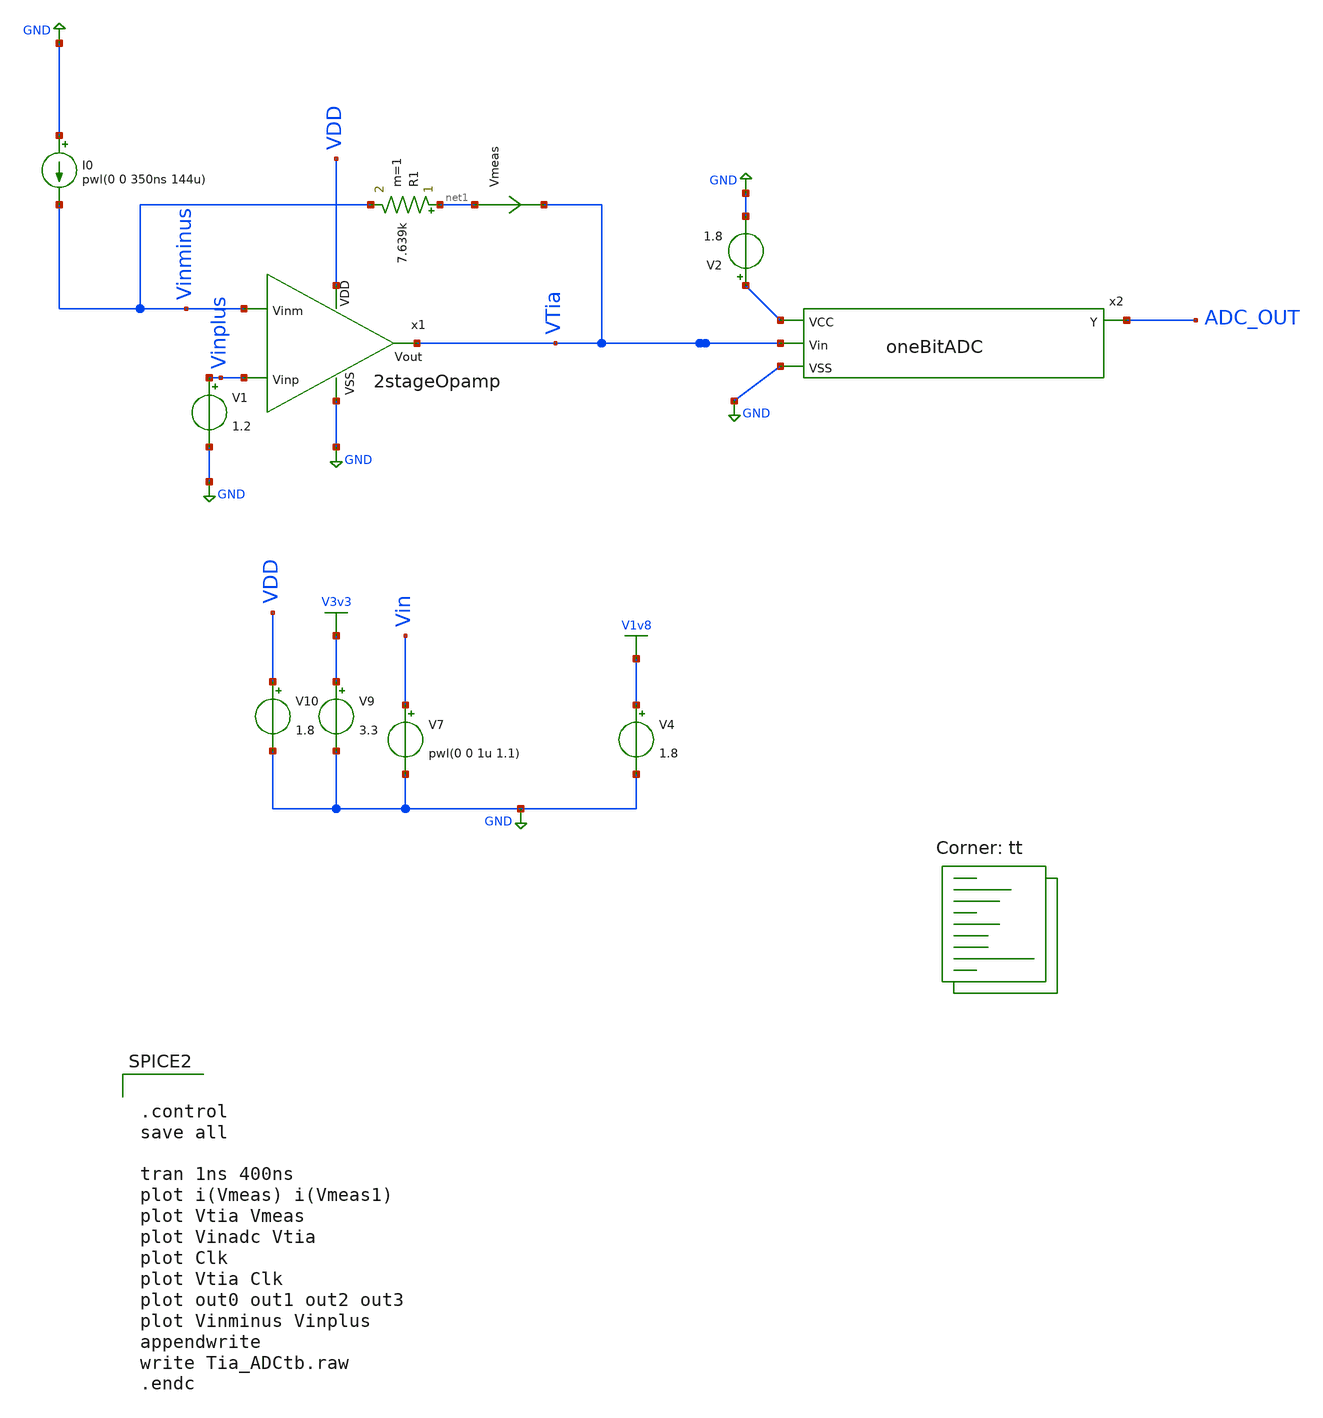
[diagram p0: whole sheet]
** sch_path: xschem/test/xschem/dec24_2stage_tbs/TIA_ADC_onebit.sch
**.subckt TIA_ADC_onebit
I0 GND Vinminus pwl(0 0 350ns 144u)
R1 net1 Vinminus 7.639k m=1
V1 Vinplus GND 1.2
Vmeas net1 VTia 0
.save i(vmeas)
x1 VDD Vinminus Vinplus VTia GND 2stageOpamp
V4 V1v8 GND 1.8
V7 Vin GND pwl(0 0 1u 1.1)
.save i(v7)
V9 V3v3 GND 3.3
V10 VDD GND 1.8
.save i(v10)
x2 net2 ADC_OUT VTia GND oneBitADC
V2 net2 GND 1.8
.save i(v2)
**** begin user architecture code
.lib $::SKYWATER_MODELS/sky130.lib.spice tt


.control
save all

tran 1ns 400ns
plot i(Vmeas) i(Vmeas1)
plot Vtia Vmeas
plot Vinadc Vtia
plot Clk
plot Vtia Clk
plot out0 out1 out2 out3
plot Vinminus Vinplus
appendwrite
write Tia_ADCtb.raw
.endc



** opencircuitdesign pdks install
.include $::SKYWATER_STDCELLS/sky130_fd_sc_hd.spice


**** end user architecture code
**.ends
.GLOBAL GND
.GLOBAL V1v8
.GLOBAL V3v3
.end
